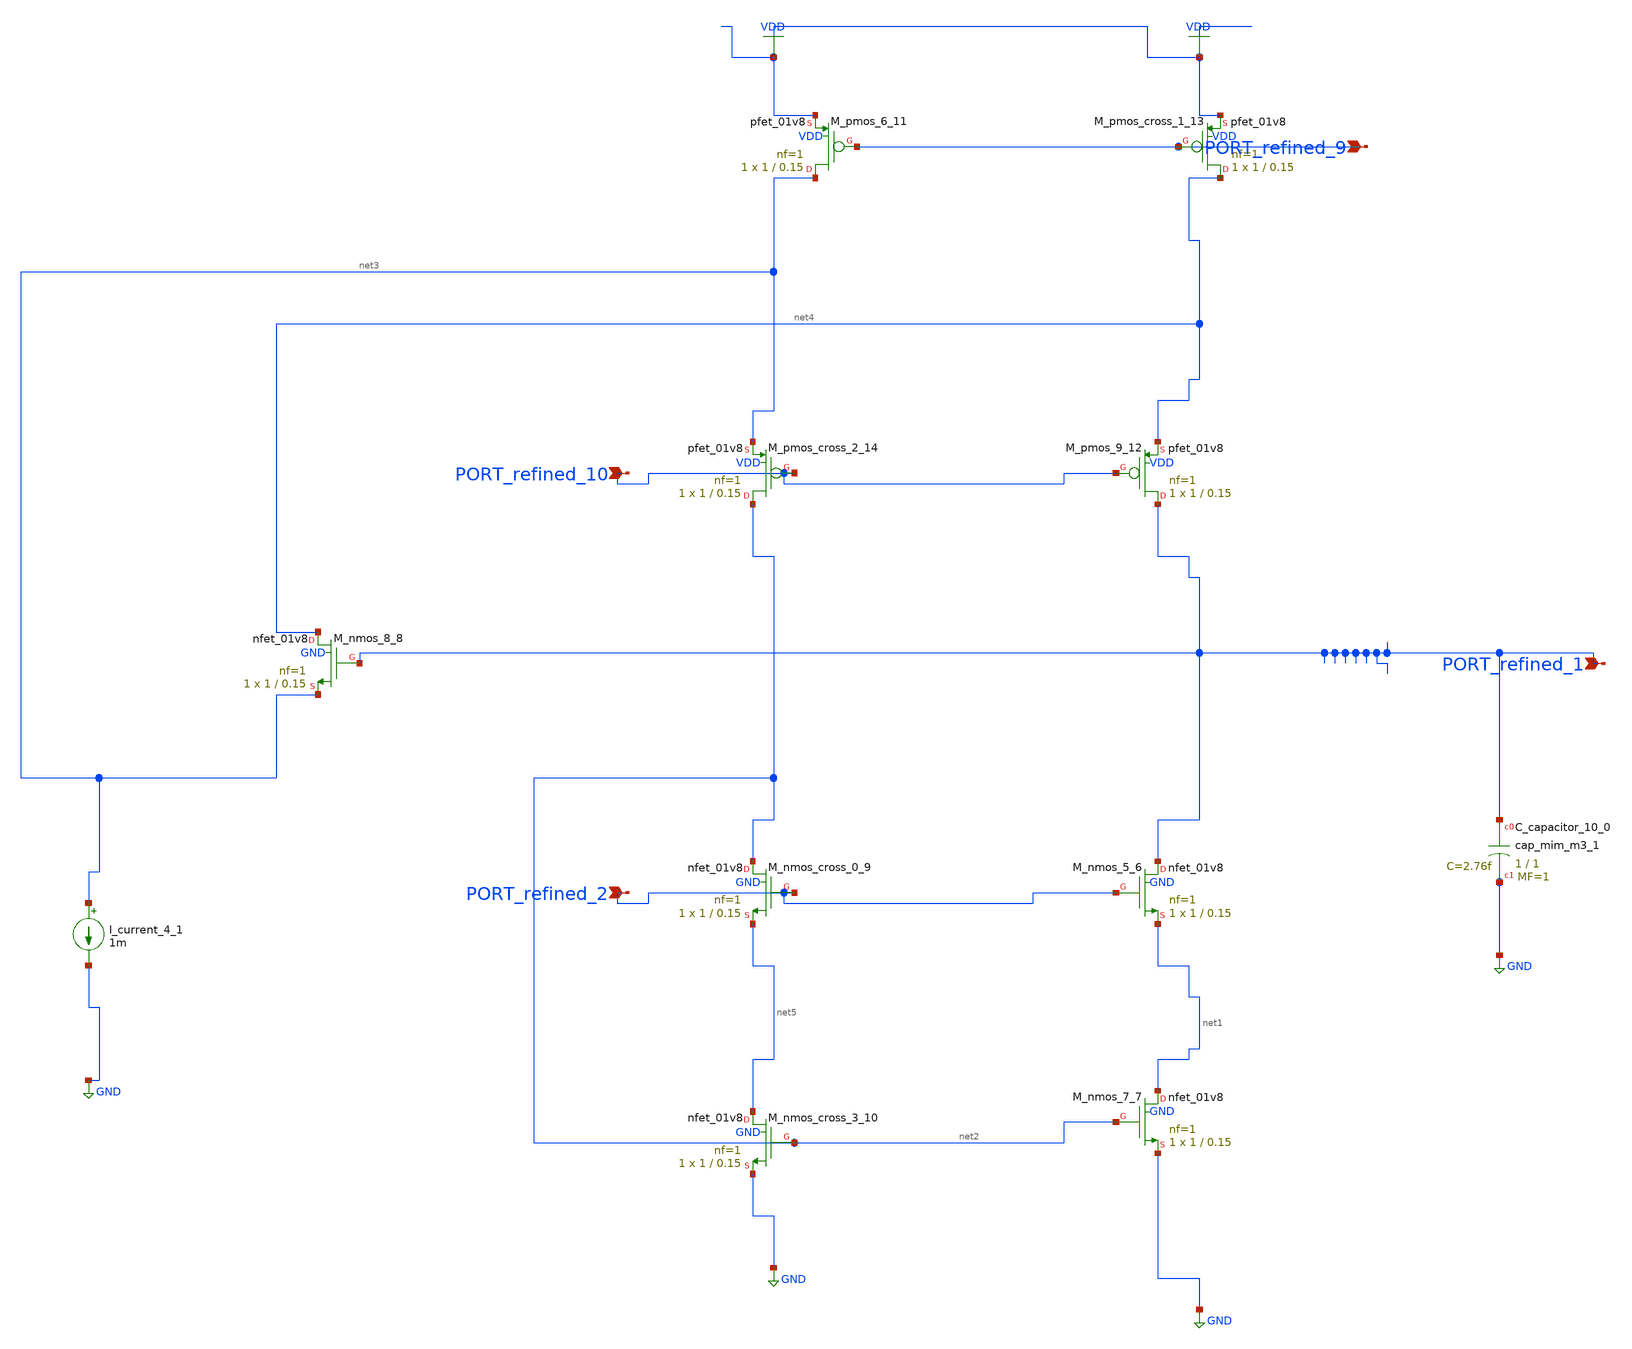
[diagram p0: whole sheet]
** sch_path: schematics/AMSNet/695.sch
**.subckt 695 PORT_refined_1 PORT_refined_2 PORT_refined_10 PORT_refined_9
*.ipin PORT_refined_1
*.ipin PORT_refined_2
*.ipin PORT_refined_10
*.ipin PORT_refined_9
XC_capacitor_10_0 PORT_refined_1 GND sky130_fd_pr__cap_mim_m3_1 W=1 L=1 MF=1 m=1
I_current_4_1 net3 GND 1m
XM_nmos_5_6 PORT_refined_1 PORT_refined_2 net1 GND sky130_fd_pr__nfet_01v8 L=0.15 W=1 nf=1 ad='int((1 + 1)/2) * 1 / 1 * 0.29'
+ as='int((1 + 2)/2) * 1 / 1 * 0.29' pd='2*int((1 + 1)/2) * (1 / 1 + 0.29)' ps='2*int((1 + 2)/2) * (1 / 1 + 0.29)'
+ nrd='0.29 / 1 ' nrs='0.29 / 1 ' sa=0 sb=0 sd=0 mult=1 m=1
XM_nmos_7_7 net1 net2 GND GND sky130_fd_pr__nfet_01v8 L=0.15 W=1 nf=1 ad='int((1 + 1)/2) * 1 / 1 * 0.29'
+ as='int((1 + 2)/2) * 1 / 1 * 0.29' pd='2*int((1 + 1)/2) * (1 / 1 + 0.29)' ps='2*int((1 + 2)/2) * (1 / 1 + 0.29)'
+ nrd='0.29 / 1 ' nrs='0.29 / 1 ' sa=0 sb=0 sd=0 mult=1 m=1
XM_nmos_8_8 net4 PORT_refined_1 net3 GND sky130_fd_pr__nfet_01v8 L=0.15 W=1 nf=1 ad='int((1 + 1)/2) * 1 / 1 * 0.29'
+ as='int((1 + 2)/2) * 1 / 1 * 0.29' pd='2*int((1 + 1)/2) * (1 / 1 + 0.29)' ps='2*int((1 + 2)/2) * (1 / 1 + 0.29)'
+ nrd='0.29 / 1 ' nrs='0.29 / 1 ' sa=0 sb=0 sd=0 mult=1 m=1
XM_nmos_cross_0_9 net2 PORT_refined_2 net5 GND sky130_fd_pr__nfet_01v8 L=0.15 W=1 nf=1 ad='int((1 + 1)/2) * 1 / 1 * 0.29'
+ as='int((1 + 2)/2) * 1 / 1 * 0.29' pd='2*int((1 + 1)/2) * (1 / 1 + 0.29)' ps='2*int((1 + 2)/2) * (1 / 1 + 0.29)'
+ nrd='0.29 / 1 ' nrs='0.29 / 1 ' sa=0 sb=0 sd=0 mult=1 m=1
XM_nmos_cross_3_10 net5 net2 GND GND sky130_fd_pr__nfet_01v8 L=0.15 W=1 nf=1 ad='int((1 + 1)/2) * 1 / 1 * 0.29'
+ as='int((1 + 2)/2) * 1 / 1 * 0.29' pd='2*int((1 + 1)/2) * (1 / 1 + 0.29)' ps='2*int((1 + 2)/2) * (1 / 1 + 0.29)'
+ nrd='0.29 / 1 ' nrs='0.29 / 1 ' sa=0 sb=0 sd=0 mult=1 m=1
XM_pmos_6_11 net3 PORT_refined_9 VDD VDD sky130_fd_pr__pfet_01v8 L=0.15 W=1 nf=1 ad='int((1 + 1)/2) * 1 / 1 * 0.29'
+ as='int((1 + 2)/2) * 1 / 1 * 0.29' pd='2*int((1 + 1)/2) * (1 / 1 + 0.29)' ps='2*int((1 + 2)/2) * (1 / 1 + 0.29)'
+ nrd='0.29 / 1 ' nrs='0.29 / 1 ' sa=0 sb=0 sd=0 mult=1 m=1
XM_pmos_9_12 PORT_refined_1 PORT_refined_10 net4 VDD sky130_fd_pr__pfet_01v8 L=0.15 W=1 nf=1 ad='int((1 + 1)/2) * 1 / 1 * 0.29'
+ as='int((1 + 2)/2) * 1 / 1 * 0.29' pd='2*int((1 + 1)/2) * (1 / 1 + 0.29)' ps='2*int((1 + 2)/2) * (1 / 1 + 0.29)'
+ nrd='0.29 / 1 ' nrs='0.29 / 1 ' sa=0 sb=0 sd=0 mult=1 m=1
XM_pmos_cross_1_13 net4 PORT_refined_9 VDD VDD sky130_fd_pr__pfet_01v8 L=0.15 W=1 nf=1 ad='int((1 + 1)/2) * 1 / 1 * 0.29'
+ as='int((1 + 2)/2) * 1 / 1 * 0.29' pd='2*int((1 + 1)/2) * (1 / 1 + 0.29)' ps='2*int((1 + 2)/2) * (1 / 1 + 0.29)'
+ nrd='0.29 / 1 ' nrs='0.29 / 1 ' sa=0 sb=0 sd=0 mult=1 m=1
XM_pmos_cross_2_14 net2 PORT_refined_10 net3 VDD sky130_fd_pr__pfet_01v8 L=0.15 W=1 nf=1 ad='int((1 + 1)/2) * 1 / 1 * 0.29'
+ as='int((1 + 2)/2) * 1 / 1 * 0.29' pd='2*int((1 + 1)/2) * (1 / 1 + 0.29)' ps='2*int((1 + 2)/2) * (1 / 1 + 0.29)'
+ nrd='0.29 / 1 ' nrs='0.29 / 1 ' sa=0 sb=0 sd=0 mult=1 m=1
**.ends
.GLOBAL GND
.GLOBAL VDD
.end
